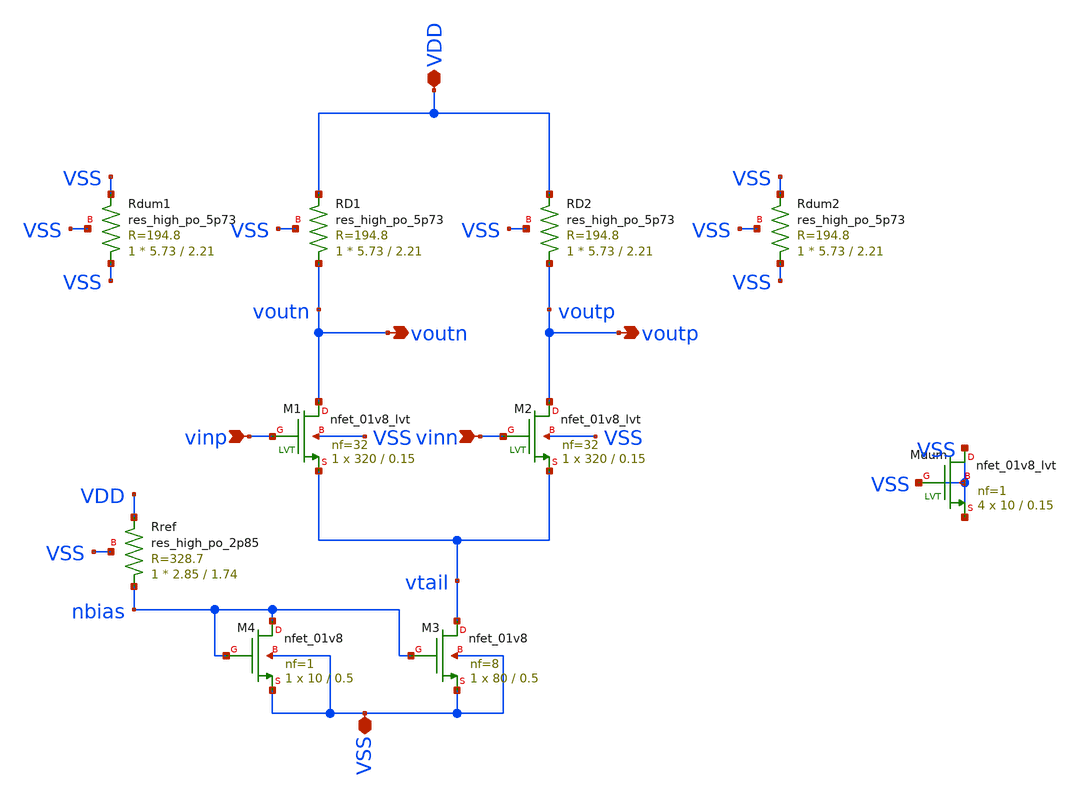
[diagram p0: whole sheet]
** sch_path: ip/bomu.sch
**.subckt bomu vinp vinn voutn voutp VDD VSS
*.ipin vinp
*.ipin vinn
*.opin voutn
*.opin voutp
*.iopin VDD
*.iopin VSS
XRD1 voutn VDD VSS sky130_fd_pr__res_high_po_5p73 L=2.21 mult=1 m=1
XRD2 voutp VDD VSS sky130_fd_pr__res_high_po_5p73 L=2.21 mult=1 m=1
XM1 voutn vinp vtail VSS sky130_fd_pr__nfet_01v8_lvt L=0.15 W=320 nf=32 ad=0 as=0 pd=0 ps=0 nrd=0
+ nrs=0 sa=0 sb=0 sd=0 mult=1 m=1
XM2 voutp vinn vtail VSS sky130_fd_pr__nfet_01v8_lvt L=0.15 W=320 nf=32 ad=0 as=0 pd=0 ps=0 nrd=0
+ nrs=0 sa=0 sb=0 sd=0 mult=1 m=1
XRref nbias VDD VSS sky130_fd_pr__res_high_po_2p85 L=1.74 mult=1 m=1
XM3 vtail nbias VSS VSS sky130_fd_pr__nfet_01v8 L=0.5 W=80 nf=8 ad=0 as=0 pd=0 ps=0 nrd=0 nrs=0 sa=0
+ sb=0 sd=0 mult=1 m=1
XM4 nbias nbias VSS VSS sky130_fd_pr__nfet_01v8 L=0.5 W=10 nf=1 ad=0 as=0 pd=0 ps=0 nrd=0 nrs=0 sa=0
+ sb=0 sd=0 mult=1 m=1
XRdum1 VSS VSS VSS sky130_fd_pr__res_high_po_5p73 L=2.21 mult=1 m=1
XRdum2 VSS VSS VSS sky130_fd_pr__res_high_po_5p73 L=2.21 mult=1 m=1
XMdum VSS VSS VSS VSS sky130_fd_pr__nfet_01v8_lvt L=0.15 W=10 nf=1 ad=0 as=0 pd=0 ps=0 nrd=0 nrs=0
+ sa=0 sb=0 sd=0 mult=4 m=4
**.ends
.end
